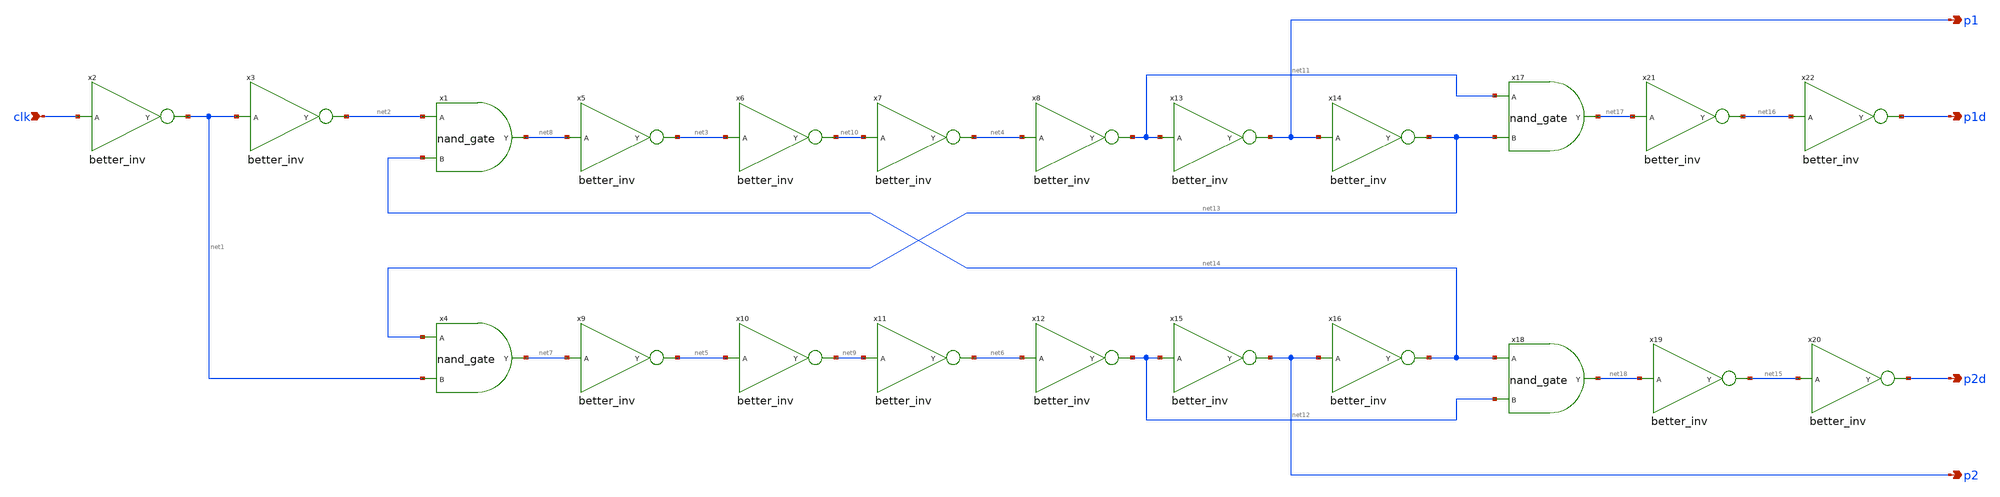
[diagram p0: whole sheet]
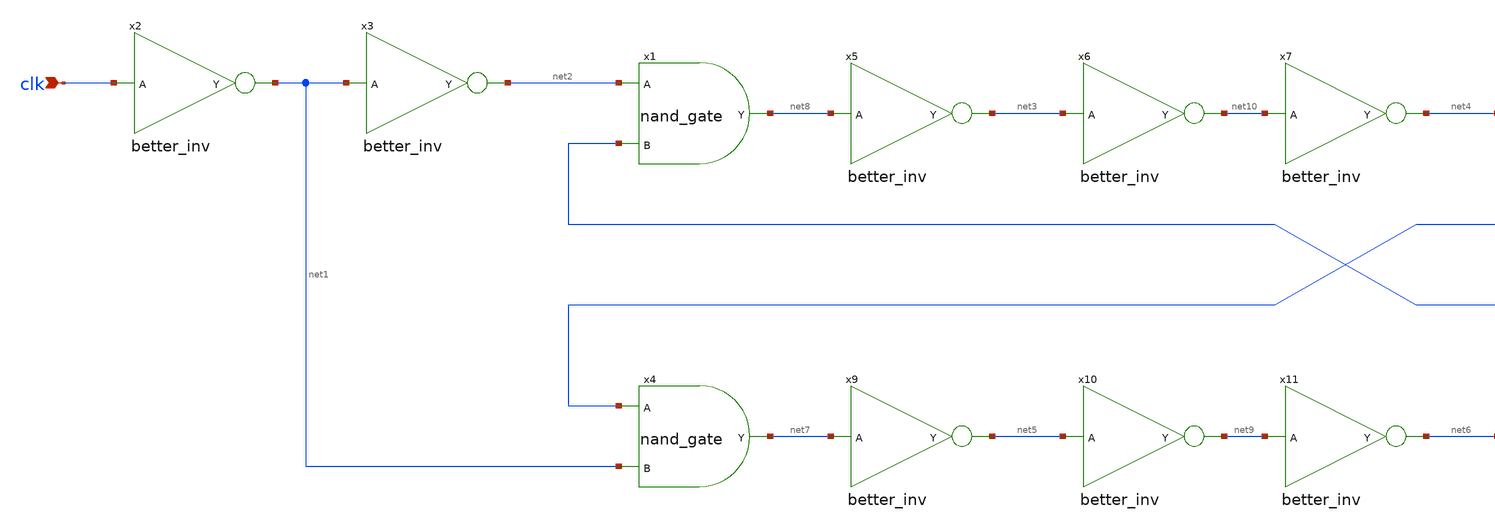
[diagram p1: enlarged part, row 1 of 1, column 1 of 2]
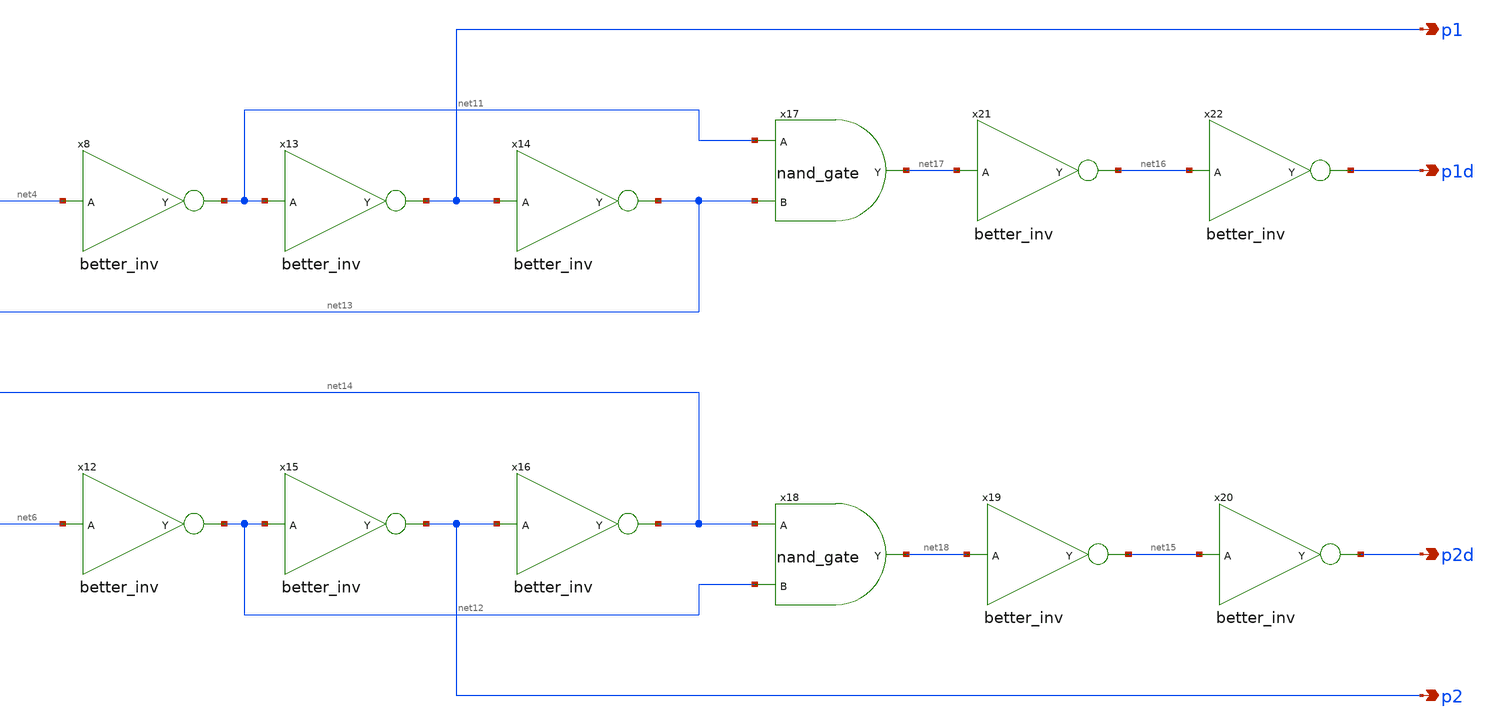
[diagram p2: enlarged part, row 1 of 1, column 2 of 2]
** sch_path: design/design_clkgen/clkgen.sch
**.subckt clkgen clk p1 p1d p2d p2
*.ipin clk
*.opin p1
*.opin p1d
*.opin p2d
*.opin p2
x1 net8 net2 net14 nand_gate
x2 net1 clk better_inv
x3 net2 net1 better_inv
x4 net7 net13 net1 nand_gate
x5 net3 net8 better_inv
x6 net10 net3 better_inv
x7 net4 net10 better_inv
x8 net11 net4 better_inv
x9 net5 net7 better_inv
x10 net9 net5 better_inv
x11 net6 net9 better_inv
x12 net12 net6 better_inv
x13 p1 net11 better_inv
x14 net13 p1 better_inv
x15 p2 net12 better_inv
x16 net14 p2 better_inv
x17 net17 net11 net13 nand_gate
x18 net18 net14 net12 nand_gate
x19 net15 net18 better_inv
x20 p2d net15 better_inv
x21 net16 net17 better_inv
x22 p1d net16 better_inv
**.ends
.end
